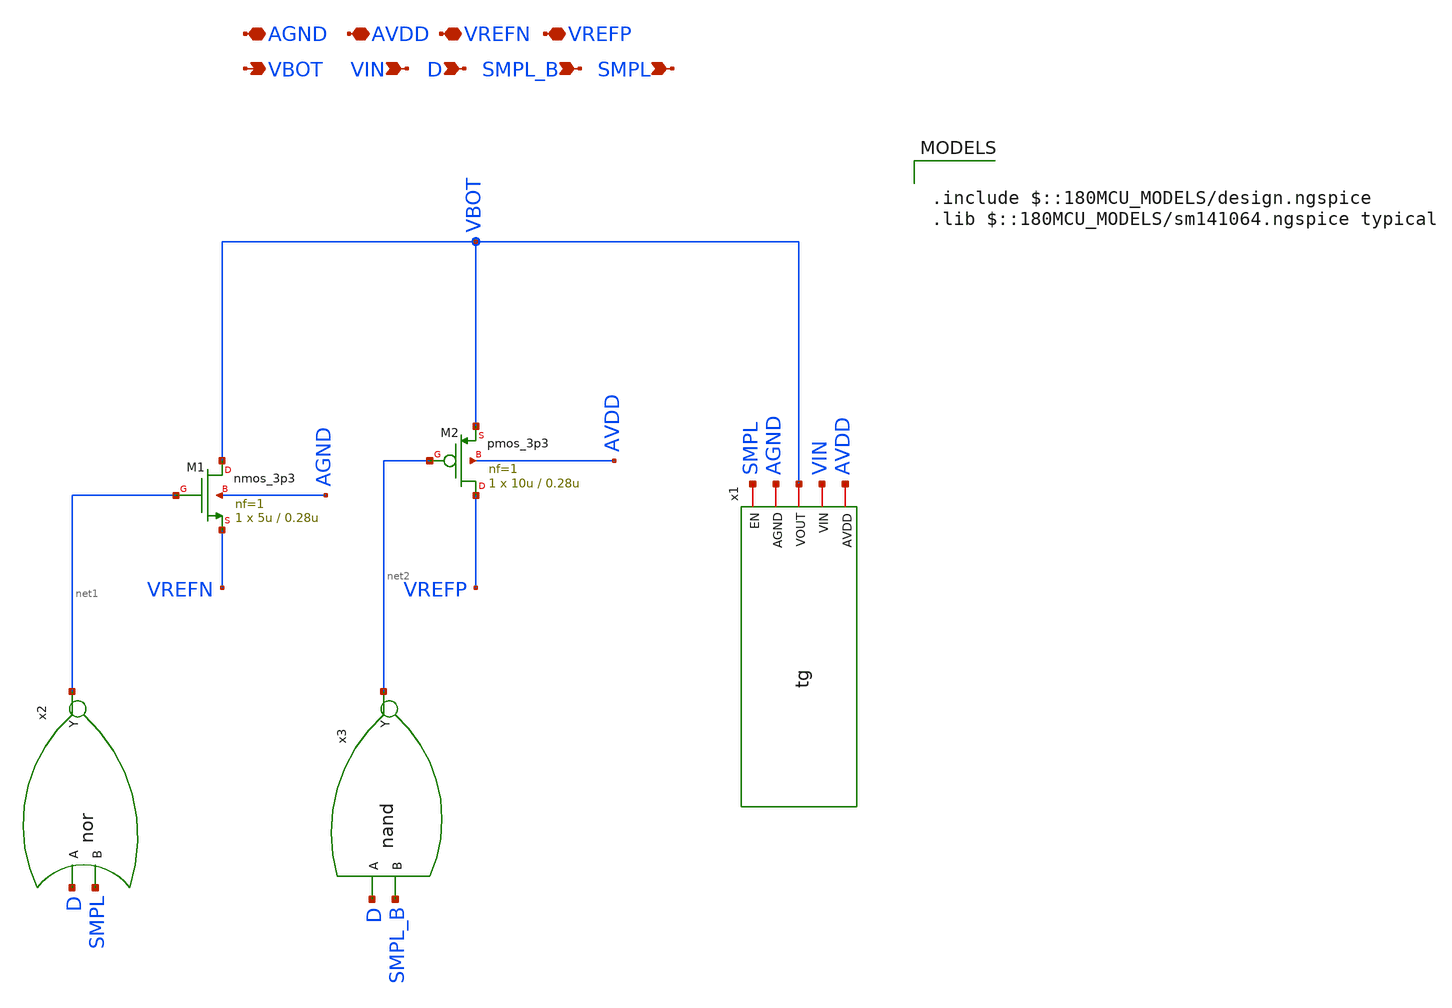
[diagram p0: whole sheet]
** sch_path: XSCHEM Files/Bottom_Plate.sch
**.subckt Bottom_Plate AGND AVDD VREFP VREFN VBOT VIN D SMPL_B SMPL
*.iopin AGND
*.iopin AVDD
*.iopin VREFP
*.iopin VREFN
*.opin VBOT
*.ipin VIN
*.ipin D
*.ipin SMPL_B
*.ipin SMPL
XM1 VBOT net1 VREFN AGND nmos_3p3 L=0.28u W=5u nf=1 ad='int((nf+1)/2) * W/nf * 0.18u' as='int((nf+2)/2) * W/nf * 0.18u'
+ pd='2*int((nf+1)/2) * (W/nf + 0.18u)' ps='2*int((nf+2)/2) * (W/nf + 0.18u)' nrd='0.18u / W' nrs='0.18u / W'
+ sa=0 sb=0 sd=0 m=1
XM2 VREFP net2 VBOT AVDD pmos_3p3 L=0.28u W=10u nf=1 ad='int((nf+1)/2) * W/nf * 0.18u' as='int((nf+2)/2) * W/nf * 0.18u'
+ pd='2*int((nf+1)/2) * (W/nf + 0.18u)' ps='2*int((nf+2)/2) * (W/nf + 0.18u)' nrd='0.18u / W' nrs='0.18u / W'
+ sa=0 sb=0 sd=0 m=1
x2 net1 D SMPL nor
x3 net2 D SMPL_B nand
x1 SMPL AGND VBOT VIN AVDD tg
**** begin user architecture code

.include $::180MCU_MODELS/design.ngspice
.lib $::180MCU_MODELS/sm141064.ngspice typical

**** end user architecture code
**.ends

* expanding   symbol:  /home/tare/Desktop/Final_1/nor.sym # of pins=3
** sym_path: XSCHEM Files/nor.sym
** sch_path: XSCHEM Files/nor.sch
.subckt nor Y A B
*.ipin A
*.opin Y
*.ipin B
**** begin user architecture code


*nor model
a1 [A b] Yi my_nor
.model my_nor d_nor(rise_delay = 1e-9 fall_delay = 1e-9                         input_load = 1e-12)

*force netlisting of digital outputs
v1 Yi Y 0


**** end user architecture code
.ends


* expanding   symbol:  /home/tare/Desktop/Final_1/nand.sym # of pins=3
** sym_path: XSCHEM Files/nand.sym
** sch_path: XSCHEM Files/nand.sch
.subckt nand Y A B
*.ipin A
*.opin Y
*.ipin B
**** begin user architecture code


*nand model
a1 [A b] Yi my_nand
.model my_nand d_nand(rise_delay = 1e-9 fall_delay = 1e-9                         input_load =
+ 1e-12)

*force netlisting of digital outputs
v1 Yi Y 0


**** end user architecture code
.ends


* expanding   symbol:  /home/tare/Desktop/last/tg.sym # of pins=5
** sym_path: XSCHEM Files/tg.sym
** sch_path: XSCHEM Files/tg.sch
.subckt tg EN AGND VOUT VIN AVDD
*.iopin AGND
*.iopin AVDD
*.iopin VOUT
*.iopin VIN
*.iopin EN
XM1 VOUT EN VIN AGND nmos_3p3 L=0.28u W=5u nf=1 ad='int((nf+1)/2) * W/nf * 0.18u' as='int((nf+2)/2) * W/nf * 0.18u'
+ pd='2*int((nf+1)/2) * (W/nf + 0.18u)' ps='2*int((nf+2)/2) * (W/nf + 0.18u)' nrd='0.18u / W' nrs='0.18u / W'
+ sa=0 sb=0 sd=0 m=1
XM2 VOUT ENB VIN AVDD pmos_3p3 L=0.28u W=10u nf=1 ad='int((nf+1)/2) * W/nf * 0.18u' as='int((nf+2)/2) * W/nf * 0.18u'
+ pd='2*int((nf+1)/2) * (W/nf + 0.18u)' ps='2*int((nf+2)/2) * (W/nf + 0.18u)' nrd='0.18u / W' nrs='0.18u / W'
+ sa=0 sb=0 sd=0 m=1
E1 ENB AVDD EN AGND -1
.ends

.end
